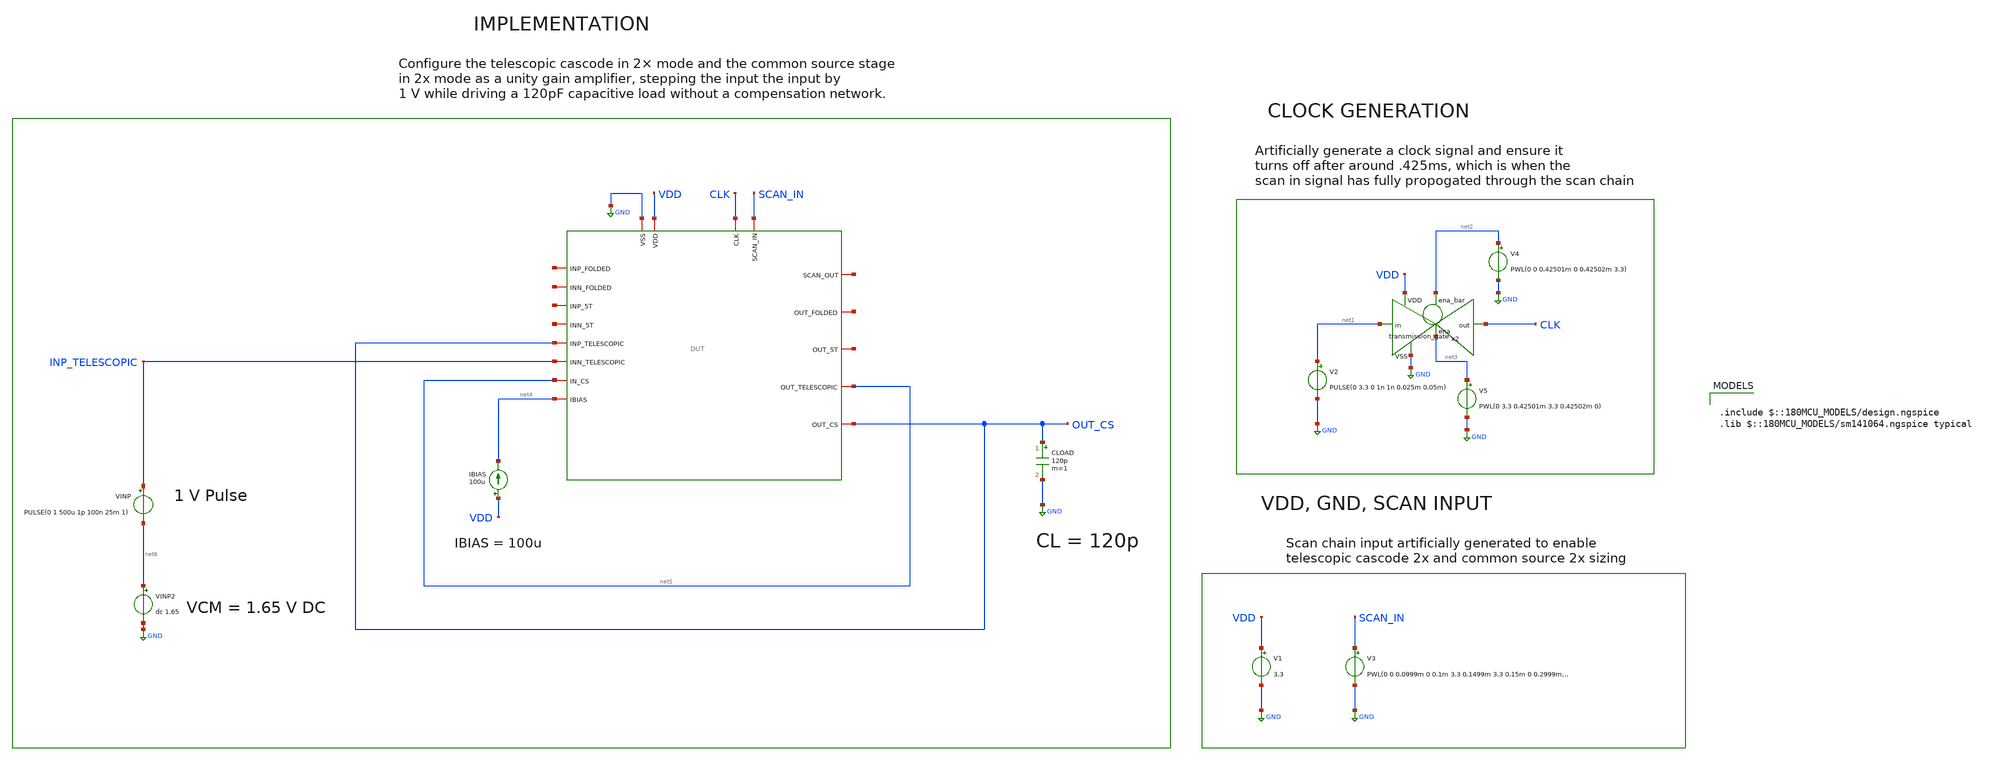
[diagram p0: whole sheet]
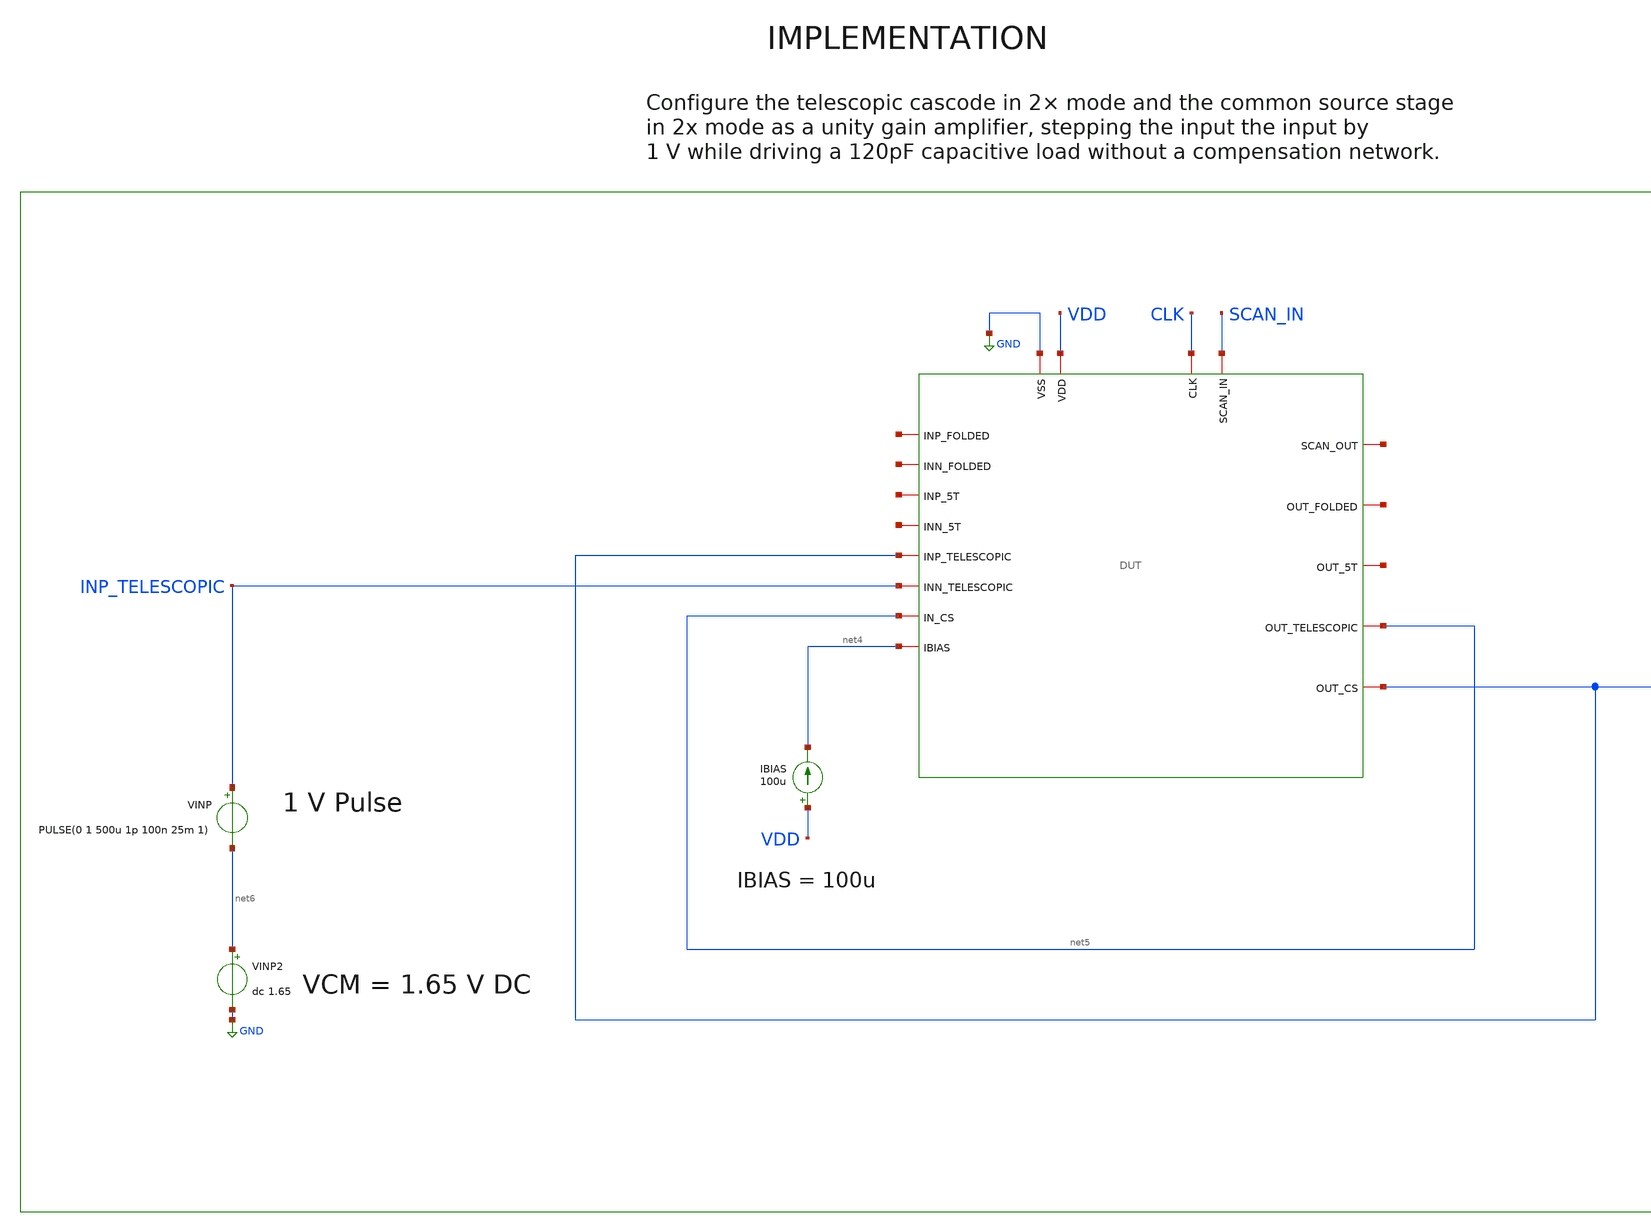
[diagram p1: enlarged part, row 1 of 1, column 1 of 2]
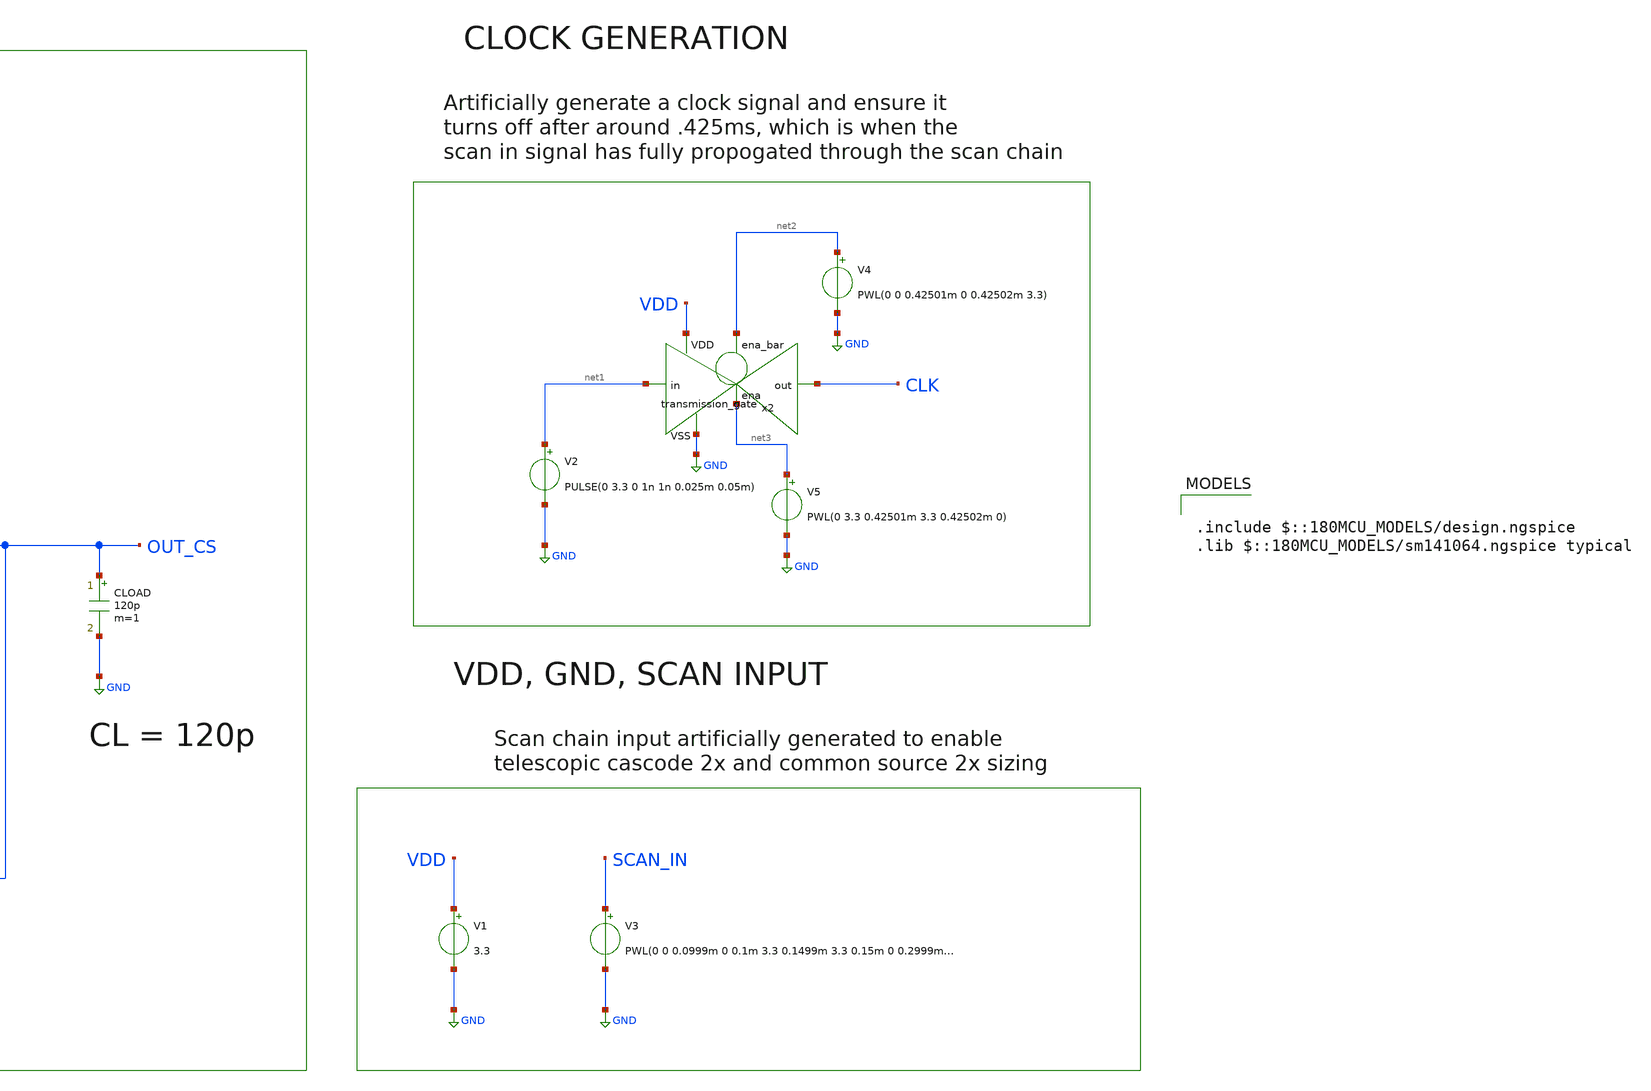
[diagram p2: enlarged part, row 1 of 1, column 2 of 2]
** sch_path: designs/libs/core_tb/mpg/ota_telescopic/2stage/Telescopic_CS_Unity Step/1V_Step_2x_2x_no_comp_tb.sch
**.subckt 1V_Step_2x_2x_no_comp_tb
V3 SCAN_IN GND PWL(0 0 0.0999m 0 0.1m 3.3 0.1499m 3.3 0.15m 0 0.2999m 0 0.3m 3.3 0.349999m 3.3 0.35m
+ 0)
V1 VDD GND 3.3
V2 net1 GND PULSE(0 3.3 0 1n 1n 0.025m 0.05m)
x2 net2 VDD CLK net1 GND net3 transmission_gate
V4 net2 GND PWL(0 0 0.42501m 0 0.42502m 3.3)
V5 net3 GND PWL(0 3.3 0.42501m 3.3 0.42502m 0)
IBIAS VDD net4 100u
CLOAD OUT_CS GND 120p m=1
x1 CLK net7 SCAN_IN GND VDD net8 net9 net10 net4 net11 net12 net13 OUT_CS net5 OUT_CS net5
+ INP_TELESCOPIC DUT
VINP INP_TELESCOPIC net6 PULSE(0 1 500u 1p 100n 25m 1)
VINP2 net6 GND dc 1.65
**** begin user architecture code

.include $::180MCU_MODELS/design.ngspice
.lib $::180MCU_MODELS/sm141064.ngspice typical



.control
set color0 = white
set color1 = black
tran 1u 2m

* Output value before the input step
meas tran v_before find v(OUT_CS) at=475u

* Output value after settling
meas tran v_after find v(OUT_CS) at=1.9m

* Calculate the 20% and 80% levels
let v_20 = v_before + 0.2*(v_after - v_before)
let v_80 = v_before + 0.8*(v_after - v_before)

* Measure crossing times after the 500 us input step
meas tran t_20 when v(OUT_CS)=v_20 rise=1 from=500u
meas tran t_80 when v(OUT_CS)=v_80 rise=1 from=500u

* Calculate slew rate
let slew_rate = (v_80 - v_20)/(t_80 - t_20)

print v_before
print v_after
print slew_rate
* Find the maximum output voltage after the input step
meas tran v_peak MAX v(OUT_CS) from=500u to=1.9m

* Overshoot voltage (peak above final value)
let overshoot = v_peak - v_after

* Percent overshoot for a 1 V step
let percent_overshoot = 100*overshoot/1

* Convert percent overshoot to decimal
let PO = percent_overshoot/100

* Damping ratio from percent overshoot
let zeta = -log(PO)/sqrt(pi*pi + log(PO)*log(PO))

* Phase margin (degrees)
let PM = atan((2*zeta)/sqrt(sqrt(1+4*zeta*zeta*zeta*zeta)-2*zeta*zeta))*180/pi

print v_peak
print overshoot
print percent_overshoot
print PM
plot v(INP_TELESCOPIC) v(OUT_CS)

.endc


**** end user architecture code
**.ends
.GLOBAL GND
.end
